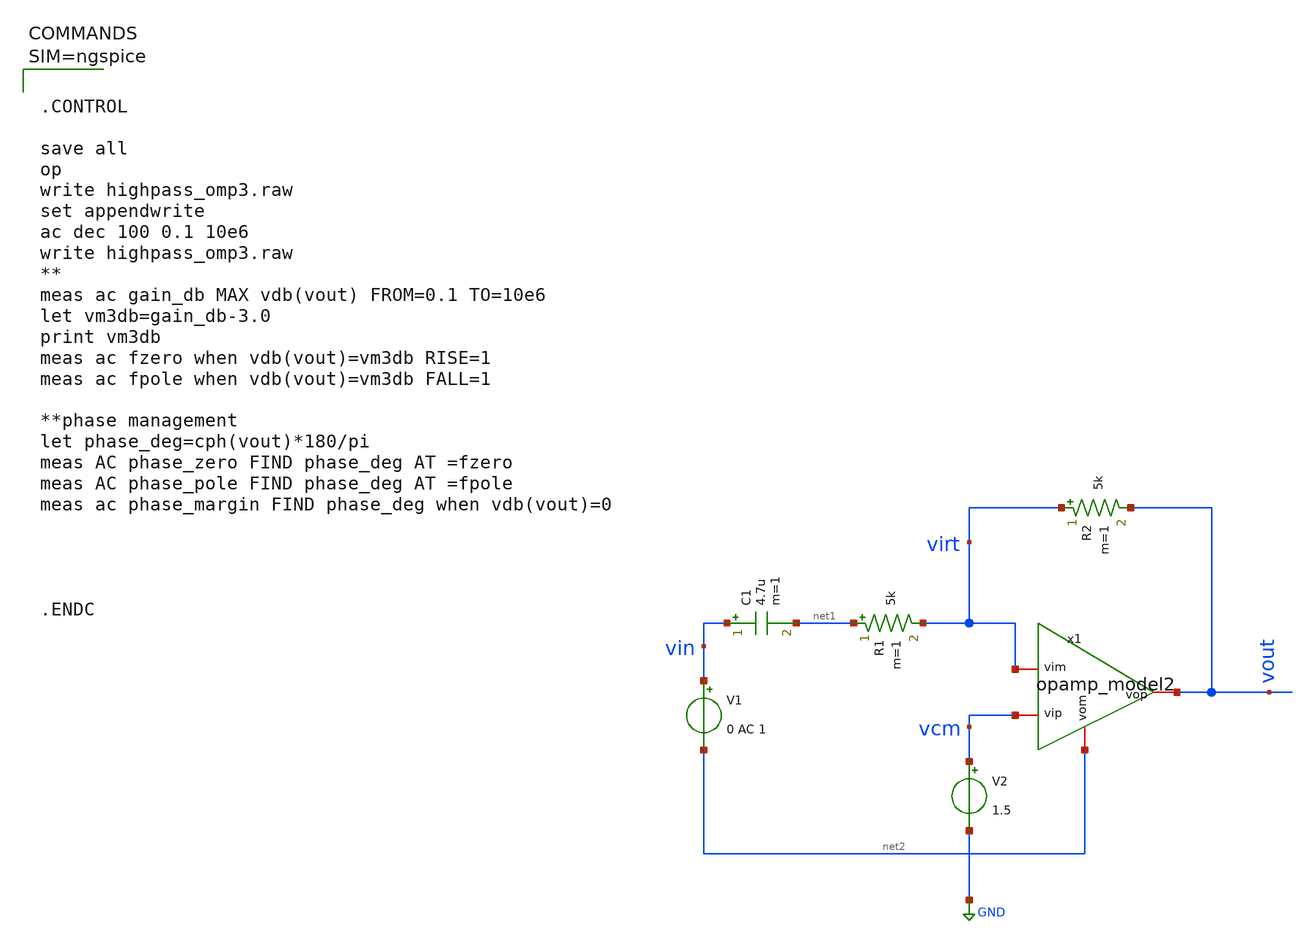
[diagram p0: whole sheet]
** sch_path: work/xschem/highpass_opamp3.sch
**.subckt highpass_opamp3
x1 vout vcm virt net2 opamp_model2
V1 vin net2 0 AC 1
R1 net1 virt 5k m=1
C1 vin net1 4.7u m=1
R2 virt vout 5k m=1
V2 vcm GND 1.5
**** begin user architecture code



.CONTROL

save all
op
write highpass_omp3.raw
set appendwrite
ac dec 100 0.1 10e6
write highpass_omp3.raw
**
meas ac gain_db MAX vdb(vout) FROM=0.1 TO=10e6
let vm3db=gain_db-3.0
print vm3db
meas ac fzero when vdb(vout)=vm3db RISE=1
meas ac fpole when vdb(vout)=vm3db FALL=1

**phase management
let phase_deg=cph(vout)*180/pi
meas AC phase_zero FIND phase_deg AT =fzero
meas AC phase_pole FIND phase_deg AT =fpole
meas ac phase_margin FIND phase_deg when vdb(vout)=0




.ENDC



**** end user architecture code
**.ends

* expanding   symbol:  opamp_model2.sym # of pins=4
** sym_path: work/xschem/opamp_model2.sym
** sch_path: work/xschem/opamp_model2.sch
.subckt opamp_model2 vop vip vim vom
*.iopin vip
*.iopin vim
*.iopin vop
*.iopin vom
E1 vop vom vip vim 1000
.ends

.GLOBAL GND
.end
